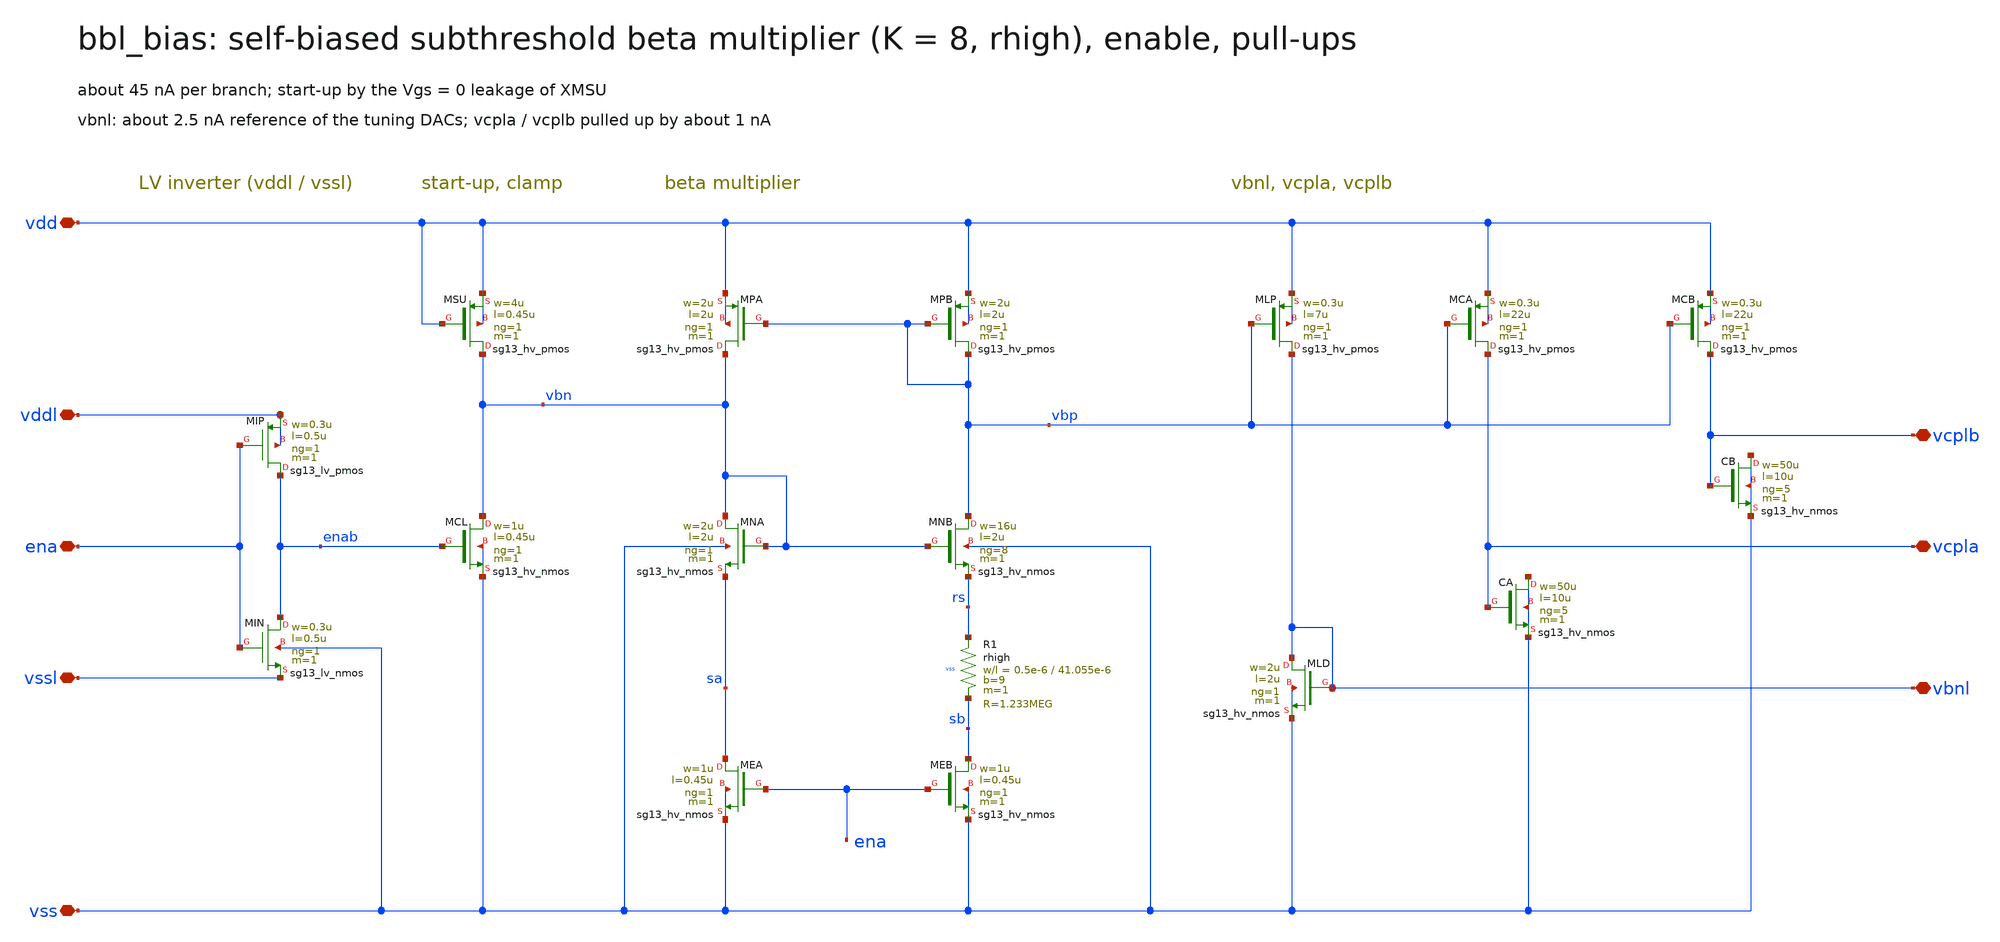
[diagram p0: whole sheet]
** sch_path: schematic/xschem/bbl_bias.sch
**.subckt bbl_bias vdd vss vddl vssl ena vbnl vcpla vcplb
*.iopin vdd
*.iopin vss
*.iopin vddl
*.iopin vssl
*.iopin ena
*.iopin vbnl
*.iopin vcpla
*.iopin vcplb
XMIP enab ena vddl vddl sg13_lv_pmos w=0.3u l=0.5u ng=1 m=1 mm_ok=1
XMIN enab ena vssl vss sg13_lv_nmos w=0.3u l=0.5u ng=1 m=1 mm_ok=1
XMSU vbn vdd vdd vdd sg13_hv_pmos w=4u l=0.45u ng=1 m=1 mm_ok=1
XMCL vbn enab vss vss sg13_hv_nmos w=1u l=0.45u ng=1 m=1 mm_ok=1
XMPA vbn vbp vdd vdd sg13_hv_pmos w=2u l=2u ng=1 m=1 mm_ok=1
XMPB vbp vbp vdd vdd sg13_hv_pmos w=2u l=2u ng=1 m=1 mm_ok=1
XMNA vbn vbn sa vss sg13_hv_nmos w=2u l=2u ng=1 m=1 mm_ok=1
XMNB vbp vbn rs vss sg13_hv_nmos w=16u l=2u ng=8 m=1 mm_ok=1
XR1 rs sb vss rhigh w=0.5e-6 l=41.055e-6 m=1 b=9 mm_ok=1
XMEA sa ena vss vss sg13_hv_nmos w=1u l=0.45u ng=1 m=1 mm_ok=1
XMEB sb ena vss vss sg13_hv_nmos w=1u l=0.45u ng=1 m=1 mm_ok=1
XMLP vbnl vbp vdd vdd sg13_hv_pmos w=0.3u l=7u ng=1 m=1 mm_ok=1
XMLD vbnl vbnl vss vss sg13_hv_nmos w=2u l=2u ng=1 m=1 mm_ok=1
XMCA vcpla vbp vdd vdd sg13_hv_pmos w=0.3u l=22u ng=1 m=1 mm_ok=1
XCA vss vcpla vss vss sg13_hv_nmos w=50u l=10u ng=5 m=1 mm_ok=1
XMCB vcplb vbp vdd vdd sg13_hv_pmos w=0.3u l=22u ng=1 m=1 mm_ok=1
XCB vss vcplb vss vss sg13_hv_nmos w=50u l=10u ng=5 m=1 mm_ok=1
**.ends
.end
